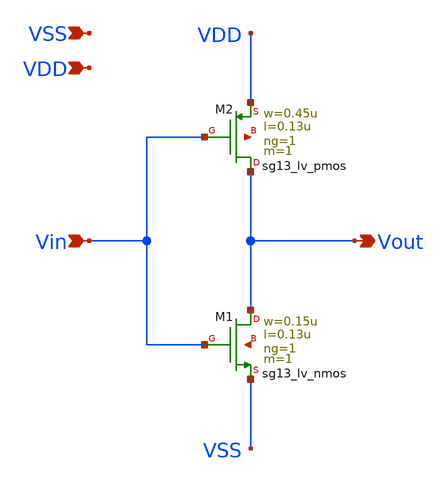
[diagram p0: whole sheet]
** sch_path: Tutoriales/INV_TUT.sch
**.subckt INV_TUT Vin Vout VSS VDD
*.ipin Vin
*.opin Vout
*.ipin VSS
*.ipin VDD
XM1 Vout Vin VSS net1 sg13_lv_nmos w=0.15u l=0.13u ng=1 m=1 mm_ok=1
XM2 Vout Vin VDD net2 sg13_lv_pmos w=0.45u l=0.13u ng=1 m=1 mm_ok=1
**.ends
.end
